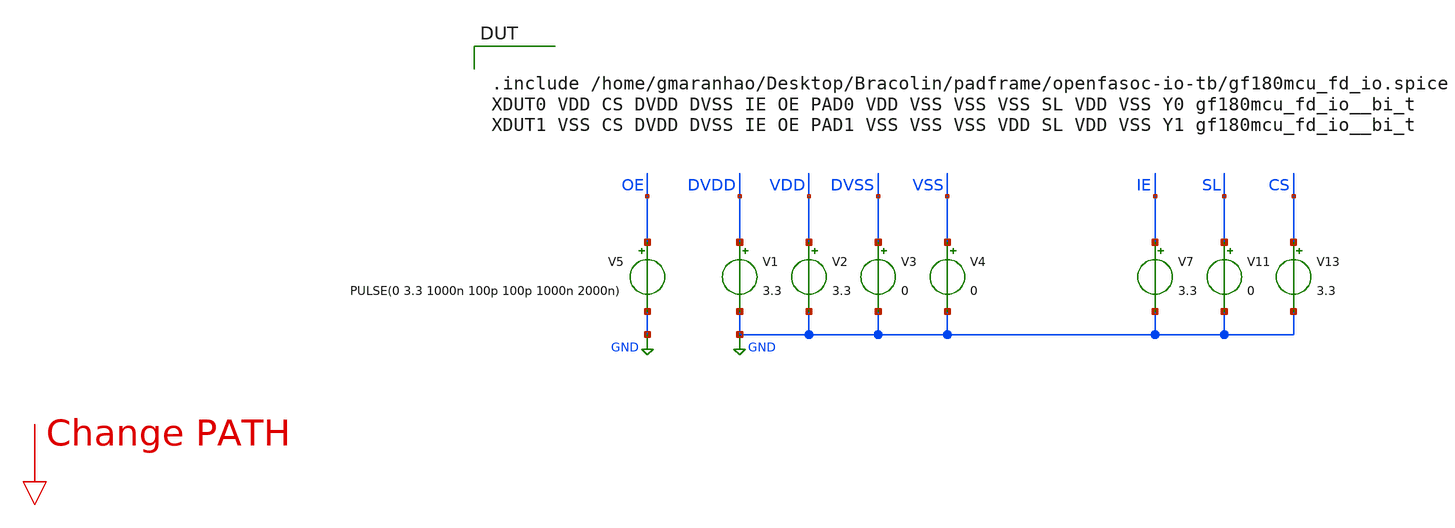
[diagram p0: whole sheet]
** sch_path: padframe/openfasoc-io-tb/digital_io_tristate.sch
**.subckt digital_io_tristate
V1 DVDD GND 3.3
V2 VDD GND 3.3
V3 DVSS GND 0
V4 VSS GND 0
V5 OE GND PULSE(0 3.3 1000n 100p 100p 1000n 2000n)
V7 IE GND 3.3
V11 SL GND 0
V13 CS GND 3.3
**** begin user architecture code


.option klu

.control
save all

tran 100p 4000n
remzerovec
write digital_io_tristate.raw

*plot OE PAD0 Y0
*plot OE PAD1 Y1
.endc



.include $::180MCU_MODELS/design.ngspice
.lib $::180MCU_MODELS/sm141064.ngspice typical
.lib $::180MCU_MODELS/sm141064.ngspice diode_typical
.lib $::180MCU_MODELS/sm141064.ngspice res_typical
.lib $::180MCU_MODELS/sm141064.ngspice mimcap_typical
.lib $::180MCU_MODELS/sm141064.ngspice moscap_typical


.include /home/gmaranhao/Desktop/Bracolin/padframe/openfasoc-io-tb/gf180mcu_fd_io.spice
XDUT0 VDD CS DVDD DVSS IE OE PAD0 VDD VSS VSS VSS SL VDD VSS Y0 gf180mcu_fd_io__bi_t
XDUT1 VSS CS DVDD DVSS IE OE PAD1 VSS VSS VSS VDD SL VDD VSS Y1 gf180mcu_fd_io__bi_t

**** end user architecture code
**.ends
.GLOBAL GND
.end
